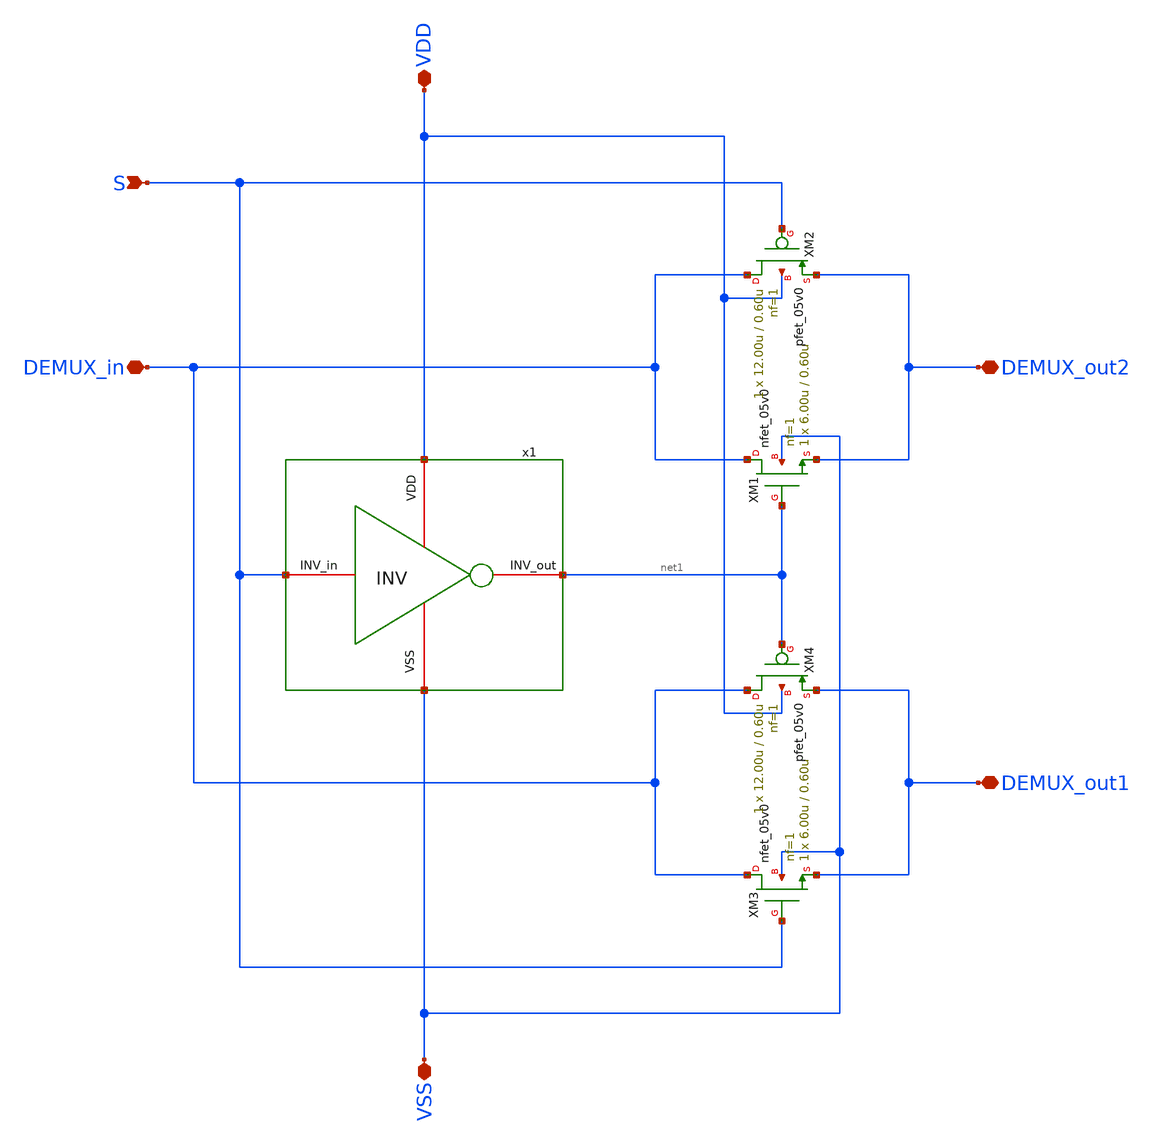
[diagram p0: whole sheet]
** sch_path: designs/libs/core_ldo/ldo/ldo_DEMUX/DEMUX.sch
**.subckt DEMUX DEMUX_out2 DEMUX_in DEMUX_out1 S VDD VSS
*.iopin DEMUX_out2
*.iopin DEMUX_in
*.iopin DEMUX_out1
*.ipin S
*.iopin VDD
*.iopin VSS
XM1 DEMUX_in net1 DEMUX_out2 VSS nfet_05v0 L=0.60u W=6.00u nf=1 ad='int((nf+1)/2) * W/nf * 0.18u' as='int((nf+2)/2) * W/nf * 0.18u'
+ pd='2*int((nf+1)/2) * (W/nf + 0.18u)' ps='2*int((nf+2)/2) * (W/nf + 0.18u)' nrd='0.18u / W' nrs='0.18u / W'
+ sa=0 sb=0 sd=0 m=1
XM2 DEMUX_in S DEMUX_out2 VDD pfet_05v0 L=0.60u W=12.00u nf=1 ad='int((nf+1)/2) * W/nf * 0.18u' as='int((nf+2)/2) * W/nf * 0.18u'
+ pd='2*int((nf+1)/2) * (W/nf + 0.18u)' ps='2*int((nf+2)/2) * (W/nf + 0.18u)' nrd='0.18u / W' nrs='0.18u / W'
+ sa=0 sb=0 sd=0 m=1
x1 VDD S net1 VSS INV
XM3 DEMUX_in S DEMUX_out1 VSS nfet_05v0 L=0.60u W=6.00u nf=1 ad='int((nf+1)/2) * W/nf * 0.18u' as='int((nf+2)/2) * W/nf * 0.18u'
+ pd='2*int((nf+1)/2) * (W/nf + 0.18u)' ps='2*int((nf+2)/2) * (W/nf + 0.18u)' nrd='0.18u / W' nrs='0.18u / W'
+ sa=0 sb=0 sd=0 m=1
XM4 DEMUX_in net1 DEMUX_out1 VDD pfet_05v0 L=0.60u W=12.00u nf=1 ad='int((nf+1)/2) * W/nf * 0.18u' as='int((nf+2)/2) * W/nf * 0.18u'
+ pd='2*int((nf+1)/2) * (W/nf + 0.18u)' ps='2*int((nf+2)/2) * (W/nf + 0.18u)' nrd='0.18u / W' nrs='0.18u / W'
+ sa=0 sb=0 sd=0 m=1
**.ends

* expanding   symbol:  libs/core_ldo/ldo/ldo_INV/INV.sym # of pins=4
** sym_path: designs/libs/core_ldo/ldo/ldo_INV/INV.sym
** sch_path: designs/libs/core_ldo/ldo/ldo_INV/INV.sch
.subckt INV VDD INV_in INV_out VSS
*.iopin INV_in
*.iopin INV_out
*.iopin VDD
*.iopin VSS
XM1 INV_out INV_in VDD VDD pfet_05v0 L=0.60u W=3.00u nf=1 ad='int((nf+1)/2) * W/nf * 0.18u' as='int((nf+2)/2) * W/nf * 0.18u'
+ pd='2*int((nf+1)/2) * (W/nf + 0.18u)' ps='2*int((nf+2)/2) * (W/nf + 0.18u)' nrd='0.18u / W' nrs='0.18u / W'
+ sa=0 sb=0 sd=0 m=1
XM2 INV_out INV_in VSS VSS nfet_05v0 L=0.60u W=1.00u nf=1 ad='int((nf+1)/2) * W/nf * 0.18u' as='int((nf+2)/2) * W/nf * 0.18u'
+ pd='2*int((nf+1)/2) * (W/nf + 0.18u)' ps='2*int((nf+2)/2) * (W/nf + 0.18u)' nrd='0.18u / W' nrs='0.18u / W'
+ sa=0 sb=0 sd=0 m=1
.ends

.end
